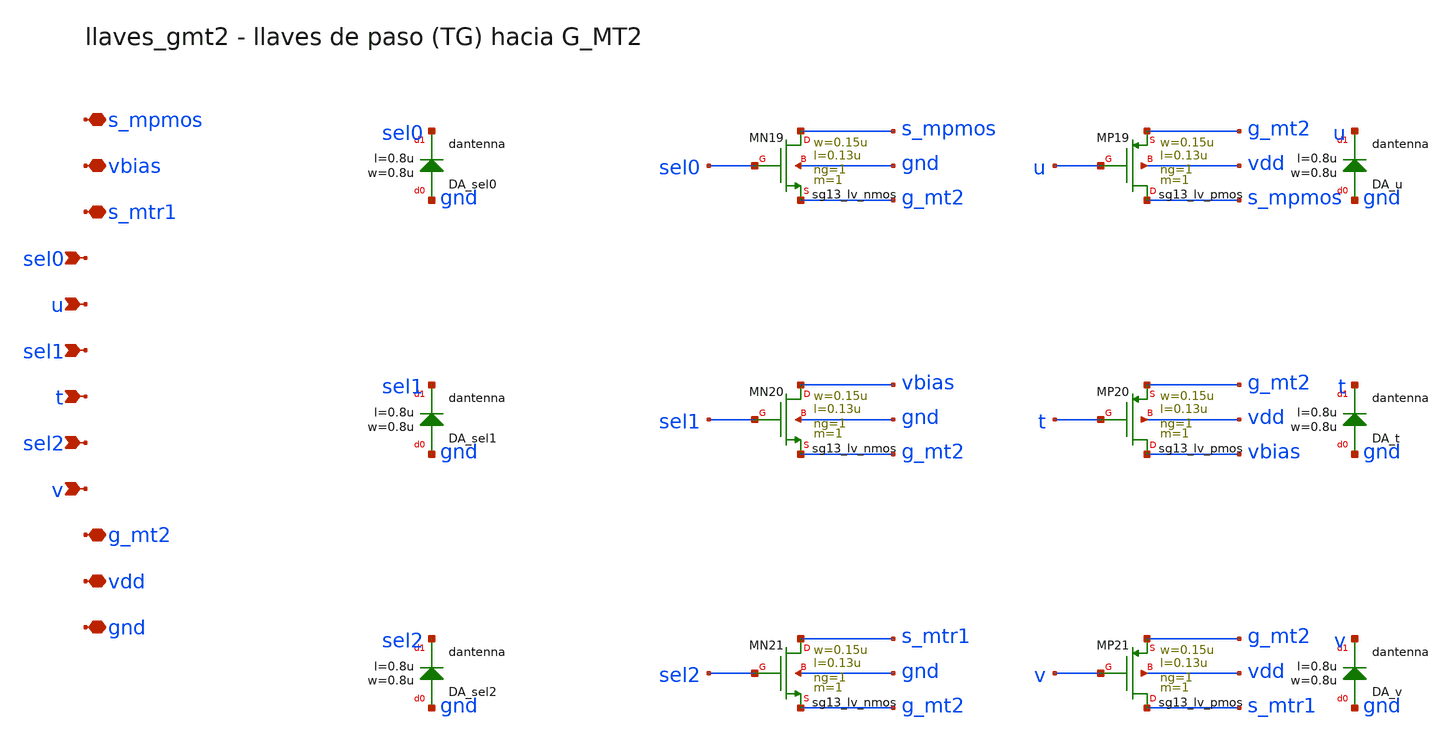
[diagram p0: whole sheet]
** sch_path: Enfoque_B/xschem/celdas/llaves_gmt2.sch
**.subckt llaves_gmt2 s_mpmos vbias s_mtr1 sel0 u sel1 t sel2 v g_mt2 vdd gnd
*.iopin s_mpmos
*.iopin vbias
*.iopin s_mtr1
*.ipin sel0
*.ipin u
*.ipin sel1
*.ipin t
*.ipin sel2
*.ipin v
*.iopin g_mt2
*.iopin vdd
*.iopin gnd
XMN19 s_mpmos sel0 g_mt2 gnd sg13_lv_nmos w=0.15u l=0.13u ng=1 m=1 mm_ok=1
XMP19 s_mpmos u g_mt2 vdd sg13_lv_pmos w=0.15u l=0.13u ng=1 m=1 mm_ok=1
XMN20 vbias sel1 g_mt2 gnd sg13_lv_nmos w=0.15u l=0.13u ng=1 m=1 mm_ok=1
XMP20 vbias t g_mt2 vdd sg13_lv_pmos w=0.15u l=0.13u ng=1 m=1 mm_ok=1
XMN21 s_mtr1 sel2 g_mt2 gnd sg13_lv_nmos w=0.15u l=0.13u ng=1 m=1 mm_ok=1
XMP21 s_mtr1 v g_mt2 vdd sg13_lv_pmos w=0.15u l=0.13u ng=1 m=1 mm_ok=1
XDA_sel0 gnd sel0 dantenna l=0.8u w=0.8u
XDA_sel1 gnd sel1 dantenna l=0.8u w=0.8u
XDA_sel2 gnd sel2 dantenna l=0.8u w=0.8u
XDA_u gnd u dantenna l=0.8u w=0.8u
XDA_t gnd t dantenna l=0.8u w=0.8u
XDA_v gnd v dantenna l=0.8u w=0.8u
**.ends
.end
